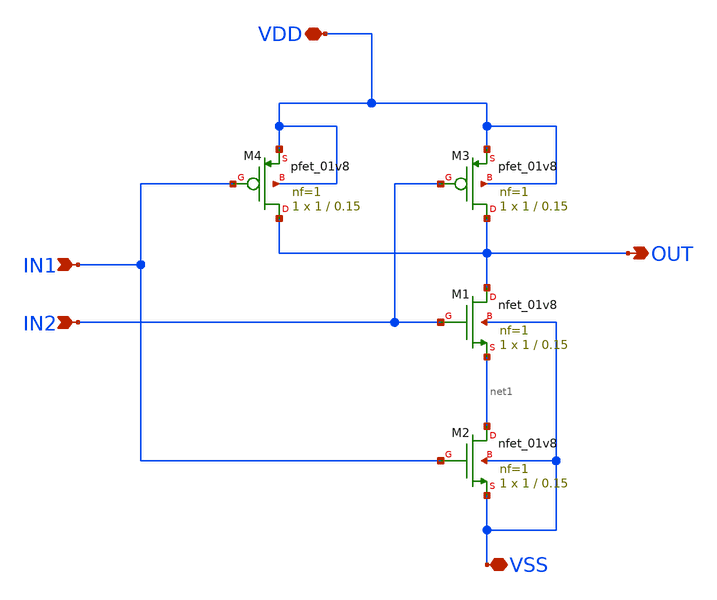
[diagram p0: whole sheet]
** sch_path: NAND/NAND.sch
**.subckt NAND IN1 IN2 VDD VSS OUT
*.ipin IN1
*.ipin IN2
*.iopin VDD
*.iopin VSS
*.opin OUT
XM1 OUT IN2 net1 VSS sky130_fd_pr__nfet_01v8 L=0.15 W=1 nf=1 ad='int((1 + 1)/2) * 1 / 1 * 0.29' as='int((1 + 2)/2) * 1 / 1 * 0.29'
+ pd='2*int((1 + 1)/2) * (1 / 1 + 0.29)' ps='2*int((1 + 2)/2) * (1 / 1 + 0.29)' nrd='0.29 / 1 ' nrs='0.29 / 1 '
+ sa=0 sb=0 sd=0 mult=1 m=1
XM2 net1 IN1 VSS VSS sky130_fd_pr__nfet_01v8 L=0.15 W=1 nf=1 ad='int((1 + 1)/2) * 1 / 1 * 0.29' as='int((1 + 2)/2) * 1 / 1 * 0.29'
+ pd='2*int((1 + 1)/2) * (1 / 1 + 0.29)' ps='2*int((1 + 2)/2) * (1 / 1 + 0.29)' nrd='0.29 / 1 ' nrs='0.29 / 1 '
+ sa=0 sb=0 sd=0 mult=1 m=1
XM3 OUT IN2 VDD VDD sky130_fd_pr__pfet_01v8 L=0.15 W=1 nf=1 ad='int((1 + 1)/2) * 1 / 1 * 0.29' as='int((1 + 2)/2) * 1 / 1 * 0.29'
+ pd='2*int((1 + 1)/2) * (1 / 1 + 0.29)' ps='2*int((1 + 2)/2) * (1 / 1 + 0.29)' nrd='0.29 / 1 ' nrs='0.29 / 1 '
+ sa=0 sb=0 sd=0 mult=1 m=1
XM4 OUT IN1 VDD VDD sky130_fd_pr__pfet_01v8 L=0.15 W=1 nf=1 ad='int((1 + 1)/2) * 1 / 1 * 0.29' as='int((1 + 2)/2) * 1 / 1 * 0.29'
+ pd='2*int((1 + 1)/2) * (1 / 1 + 0.29)' ps='2*int((1 + 2)/2) * (1 / 1 + 0.29)' nrd='0.29 / 1 ' nrs='0.29 / 1 '
+ sa=0 sb=0 sd=0 mult=1 m=1
**.ends
.end
